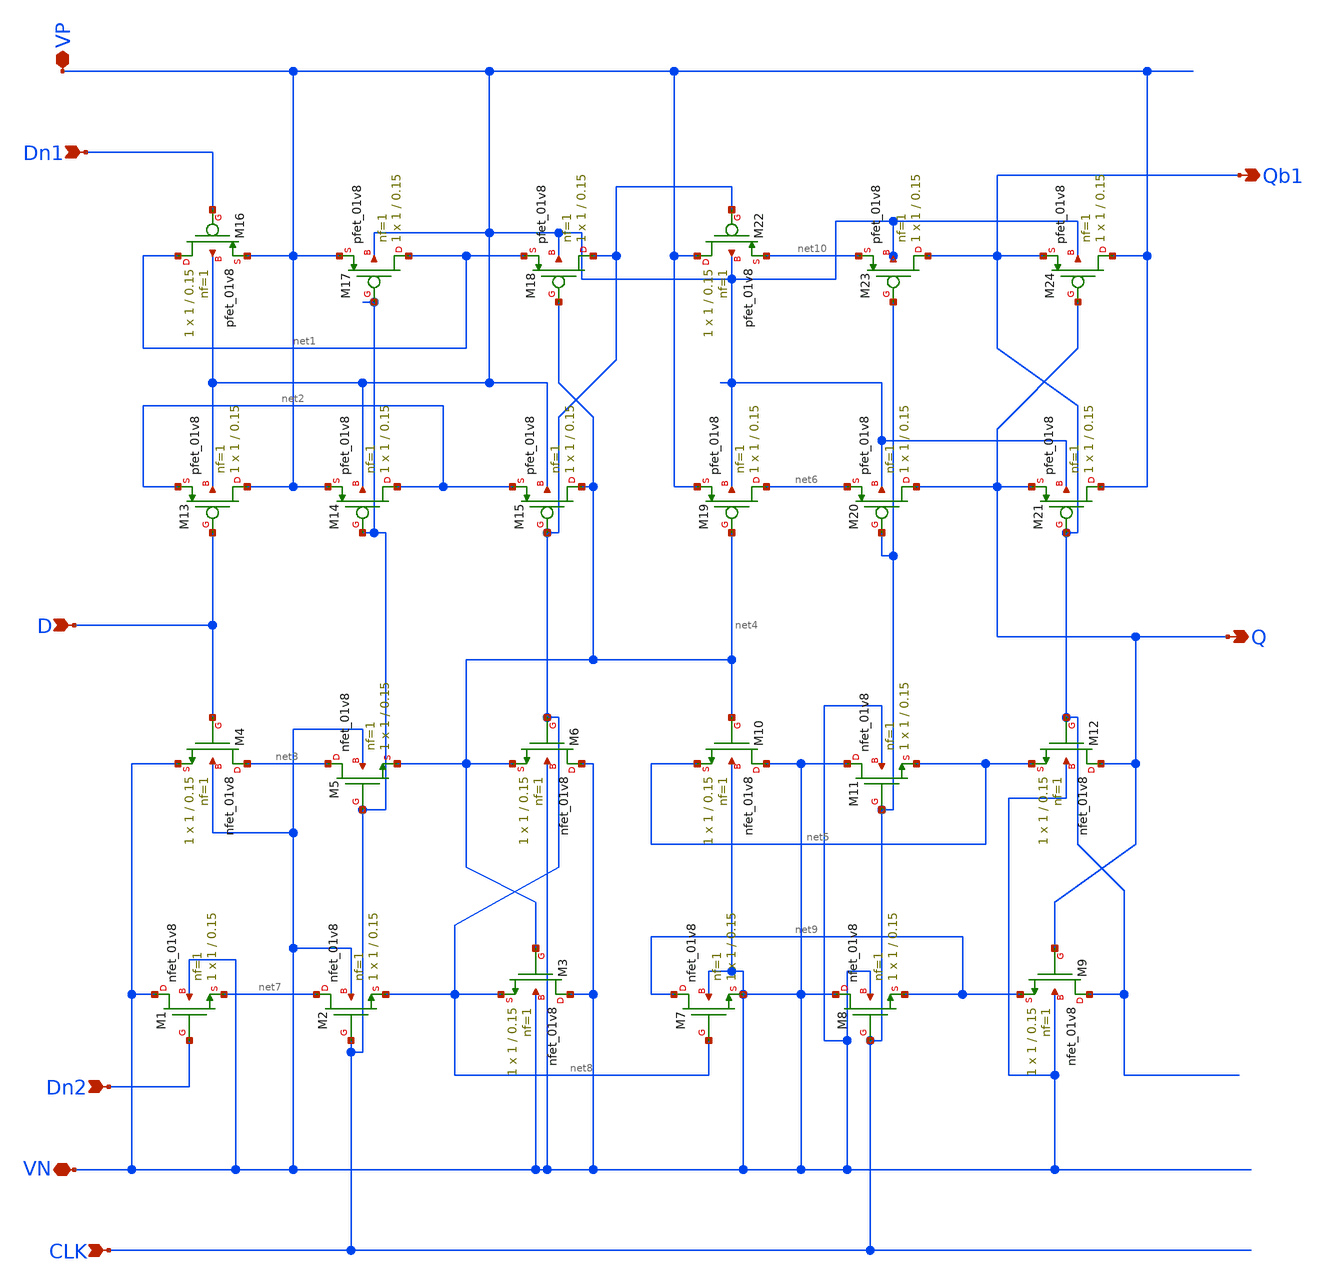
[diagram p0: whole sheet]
** sch_path: d-flipflop.sch
**.subckt d-flipflop D Dn1 Qb1 Q CLK Dn2 VP VN
*.ipin D
*.ipin Dn1
*.opin Qb1
*.opin Q
*.ipin CLK
*.ipin Dn2
*.iopin VP
*.iopin VN
XM1 VN Dn2 net7 VN sky130_fd_pr__nfet_01v8 L=0.15 W=1 nf=1 ad='int((nf+1)/2) * W/nf * 0.29' as='int((nf+2)/2) * W/nf * 0.29'
+ pd='2*int((nf+1)/2) * (W/nf + 0.29)' ps='2*int((nf+2)/2) * (W/nf + 0.29)' nrd='0.29 / W' nrs='0.29 / W'
+ sa=0 sb=0 sd=0 mult=1 m=1
XM2 net7 CLK net8 VN sky130_fd_pr__nfet_01v8 L=0.15 W=1 nf=1 ad='int((nf+1)/2) * W/nf * 0.29' as='int((nf+2)/2) * W/nf * 0.29'
+ pd='2*int((nf+1)/2) * (W/nf + 0.29)' ps='2*int((nf+2)/2) * (W/nf + 0.29)' nrd='0.29 / W' nrs='0.29 / W'
+ sa=0 sb=0 sd=0 mult=1 m=1
XM3 VN net4 net8 VN sky130_fd_pr__nfet_01v8 L=0.15 W=1 nf=1 ad='int((nf+1)/2) * W/nf * 0.29' as='int((nf+2)/2) * W/nf * 0.29'
+ pd='2*int((nf+1)/2) * (W/nf + 0.29)' ps='2*int((nf+2)/2) * (W/nf + 0.29)' nrd='0.29 / W' nrs='0.29 / W'
+ sa=0 sb=0 sd=0 mult=1 m=1
XM4 net3 D VN VN sky130_fd_pr__nfet_01v8 L=0.15 W=1 nf=1 ad='int((nf+1)/2) * W/nf * 0.29' as='int((nf+2)/2) * W/nf * 0.29'
+ pd='2*int((nf+1)/2) * (W/nf + 0.29)' ps='2*int((nf+2)/2) * (W/nf + 0.29)' nrd='0.29 / W' nrs='0.29 / W'
+ sa=0 sb=0 sd=0 mult=1 m=1
XM5 net3 CLK net4 VN sky130_fd_pr__nfet_01v8 L=0.15 W=1 nf=1 ad='int((nf+1)/2) * W/nf * 0.29' as='int((nf+2)/2) * W/nf * 0.29'
+ pd='2*int((nf+1)/2) * (W/nf + 0.29)' ps='2*int((nf+2)/2) * (W/nf + 0.29)' nrd='0.29 / W' nrs='0.29 / W'
+ sa=0 sb=0 sd=0 mult=1 m=1
XM6 VN net8 net4 VN sky130_fd_pr__nfet_01v8 L=0.15 W=1 nf=1 ad='int((nf+1)/2) * W/nf * 0.29' as='int((nf+2)/2) * W/nf * 0.29'
+ pd='2*int((nf+1)/2) * (W/nf + 0.29)' ps='2*int((nf+2)/2) * (W/nf + 0.29)' nrd='0.29 / W' nrs='0.29 / W'
+ sa=0 sb=0 sd=0 mult=1 m=1
XM7 net9 net8 VN VN sky130_fd_pr__nfet_01v8 L=0.15 W=1 nf=1 ad='int((nf+1)/2) * W/nf * 0.29' as='int((nf+2)/2) * W/nf * 0.29'
+ pd='2*int((nf+1)/2) * (W/nf + 0.29)' ps='2*int((nf+2)/2) * (W/nf + 0.29)' nrd='0.29 / W' nrs='0.29 / W'
+ sa=0 sb=0 sd=0 mult=1 m=1
XM8 VN CLK net9 VN sky130_fd_pr__nfet_01v8 L=0.15 W=1 nf=1 ad='int((nf+1)/2) * W/nf * 0.29' as='int((nf+2)/2) * W/nf * 0.29'
+ pd='2*int((nf+1)/2) * (W/nf + 0.29)' ps='2*int((nf+2)/2) * (W/nf + 0.29)' nrd='0.29 / W' nrs='0.29 / W'
+ sa=0 sb=0 sd=0 mult=1 m=1
XM9 Qb1 Q net9 VN sky130_fd_pr__nfet_01v8 L=0.15 W=1 nf=1 ad='int((nf+1)/2) * W/nf * 0.29' as='int((nf+2)/2) * W/nf * 0.29'
+ pd='2*int((nf+1)/2) * (W/nf + 0.29)' ps='2*int((nf+2)/2) * (W/nf + 0.29)' nrd='0.29 / W' nrs='0.29 / W'
+ sa=0 sb=0 sd=0 mult=1 m=1
XM10 VN net4 net5 VN sky130_fd_pr__nfet_01v8 L=0.15 W=1 nf=1 ad='int((nf+1)/2) * W/nf * 0.29' as='int((nf+2)/2) * W/nf * 0.29'
+ pd='2*int((nf+1)/2) * (W/nf + 0.29)' ps='2*int((nf+2)/2) * (W/nf + 0.29)' nrd='0.29 / W' nrs='0.29 / W'
+ sa=0 sb=0 sd=0 mult=1 m=1
XM11 VN CLK net5 VN sky130_fd_pr__nfet_01v8 L=0.15 W=1 nf=1 ad='int((nf+1)/2) * W/nf * 0.29' as='int((nf+2)/2) * W/nf * 0.29'
+ pd='2*int((nf+1)/2) * (W/nf + 0.29)' ps='2*int((nf+2)/2) * (W/nf + 0.29)' nrd='0.29 / W' nrs='0.29 / W'
+ sa=0 sb=0 sd=0 mult=1 m=1
XM12 Q Qb1 net5 VN sky130_fd_pr__nfet_01v8 L=0.15 W=1 nf=1 ad='int((nf+1)/2) * W/nf * 0.29' as='int((nf+2)/2) * W/nf * 0.29'
+ pd='2*int((nf+1)/2) * (W/nf + 0.29)' ps='2*int((nf+2)/2) * (W/nf + 0.29)' nrd='0.29 / W' nrs='0.29 / W'
+ sa=0 sb=0 sd=0 mult=1 m=1
XM13 VP D net2 VP sky130_fd_pr__pfet_01v8 L=0.15 W=1 nf=1 ad='int((nf+1)/2) * W/nf * 0.29' as='int((nf+2)/2) * W/nf * 0.29'
+ pd='2*int((nf+1)/2) * (W/nf + 0.29)' ps='2*int((nf+2)/2) * (W/nf + 0.29)' nrd='0.29 / W' nrs='0.29 / W'
+ sa=0 sb=0 sd=0 mult=1 m=1
XM14 net2 CLK VP VP sky130_fd_pr__pfet_01v8 L=0.15 W=1 nf=1 ad='int((nf+1)/2) * W/nf * 0.29' as='int((nf+2)/2) * W/nf * 0.29'
+ pd='2*int((nf+1)/2) * (W/nf + 0.29)' ps='2*int((nf+2)/2) * (W/nf + 0.29)' nrd='0.29 / W' nrs='0.29 / W'
+ sa=0 sb=0 sd=0 mult=1 m=1
XM15 net4 net8 net2 VP sky130_fd_pr__pfet_01v8 L=0.15 W=1 nf=1 ad='int((nf+1)/2) * W/nf * 0.29' as='int((nf+2)/2) * W/nf * 0.29'
+ pd='2*int((nf+1)/2) * (W/nf + 0.29)' ps='2*int((nf+2)/2) * (W/nf + 0.29)' nrd='0.29 / W' nrs='0.29 / W'
+ sa=0 sb=0 sd=0 mult=1 m=1
XM16 net1 Dn1 VP VP sky130_fd_pr__pfet_01v8 L=0.15 W=1 nf=1 ad='int((nf+1)/2) * W/nf * 0.29' as='int((nf+2)/2) * W/nf * 0.29'
+ pd='2*int((nf+1)/2) * (W/nf + 0.29)' ps='2*int((nf+2)/2) * (W/nf + 0.29)' nrd='0.29 / W' nrs='0.29 / W'
+ sa=0 sb=0 sd=0 mult=1 m=1
XM17 net1 CLK VP VP sky130_fd_pr__pfet_01v8 L=0.15 W=1 nf=1 ad='int((nf+1)/2) * W/nf * 0.29' as='int((nf+2)/2) * W/nf * 0.29'
+ pd='2*int((nf+1)/2) * (W/nf + 0.29)' ps='2*int((nf+2)/2) * (W/nf + 0.29)' nrd='0.29 / W' nrs='0.29 / W'
+ sa=0 sb=0 sd=0 mult=1 m=1
XM18 net8 net4 net1 VP sky130_fd_pr__pfet_01v8 L=0.15 W=1 nf=1 ad='int((nf+1)/2) * W/nf * 0.29' as='int((nf+2)/2) * W/nf * 0.29'
+ pd='2*int((nf+1)/2) * (W/nf + 0.29)' ps='2*int((nf+2)/2) * (W/nf + 0.29)' nrd='0.29 / W' nrs='0.29 / W'
+ sa=0 sb=0 sd=0 mult=1 m=1
XM19 net6 net4 VP VP sky130_fd_pr__pfet_01v8 L=0.15 W=1 nf=1 ad='int((nf+1)/2) * W/nf * 0.29' as='int((nf+2)/2) * W/nf * 0.29'
+ pd='2*int((nf+1)/2) * (W/nf + 0.29)' ps='2*int((nf+2)/2) * (W/nf + 0.29)' nrd='0.29 / W' nrs='0.29 / W'
+ sa=0 sb=0 sd=0 mult=1 m=1
XM20 Q CLK net6 VP sky130_fd_pr__pfet_01v8 L=0.15 W=1 nf=1 ad='int((nf+1)/2) * W/nf * 0.29' as='int((nf+2)/2) * W/nf * 0.29'
+ pd='2*int((nf+1)/2) * (W/nf + 0.29)' ps='2*int((nf+2)/2) * (W/nf + 0.29)' nrd='0.29 / W' nrs='0.29 / W'
+ sa=0 sb=0 sd=0 mult=1 m=1
XM21 VP Qb1 Q VP sky130_fd_pr__pfet_01v8 L=0.15 W=1 nf=1 ad='int((nf+1)/2) * W/nf * 0.29' as='int((nf+2)/2) * W/nf * 0.29'
+ pd='2*int((nf+1)/2) * (W/nf + 0.29)' ps='2*int((nf+2)/2) * (W/nf + 0.29)' nrd='0.29 / W' nrs='0.29 / W'
+ sa=0 sb=0 sd=0 mult=1 m=1
XM22 VP net8 net10 VP sky130_fd_pr__pfet_01v8 L=0.15 W=1 nf=1 ad='int((nf+1)/2) * W/nf * 0.29' as='int((nf+2)/2) * W/nf * 0.29'
+ pd='2*int((nf+1)/2) * (W/nf + 0.29)' ps='2*int((nf+2)/2) * (W/nf + 0.29)' nrd='0.29 / W' nrs='0.29 / W'
+ sa=0 sb=0 sd=0 mult=1 m=1
XM23 Qb1 CLK net10 VP sky130_fd_pr__pfet_01v8 L=0.15 W=1 nf=1 ad='int((nf+1)/2) * W/nf * 0.29' as='int((nf+2)/2) * W/nf * 0.29'
+ pd='2*int((nf+1)/2) * (W/nf + 0.29)' ps='2*int((nf+2)/2) * (W/nf + 0.29)' nrd='0.29 / W' nrs='0.29 / W'
+ sa=0 sb=0 sd=0 mult=1 m=1
XM24 VP Q Qb1 VP sky130_fd_pr__pfet_01v8 L=0.15 W=1 nf=1 ad='int((nf+1)/2) * W/nf * 0.29' as='int((nf+2)/2) * W/nf * 0.29'
+ pd='2*int((nf+1)/2) * (W/nf + 0.29)' ps='2*int((nf+2)/2) * (W/nf + 0.29)' nrd='0.29 / W' nrs='0.29 / W'
+ sa=0 sb=0 sd=0 mult=1 m=1
**.ends
.end
